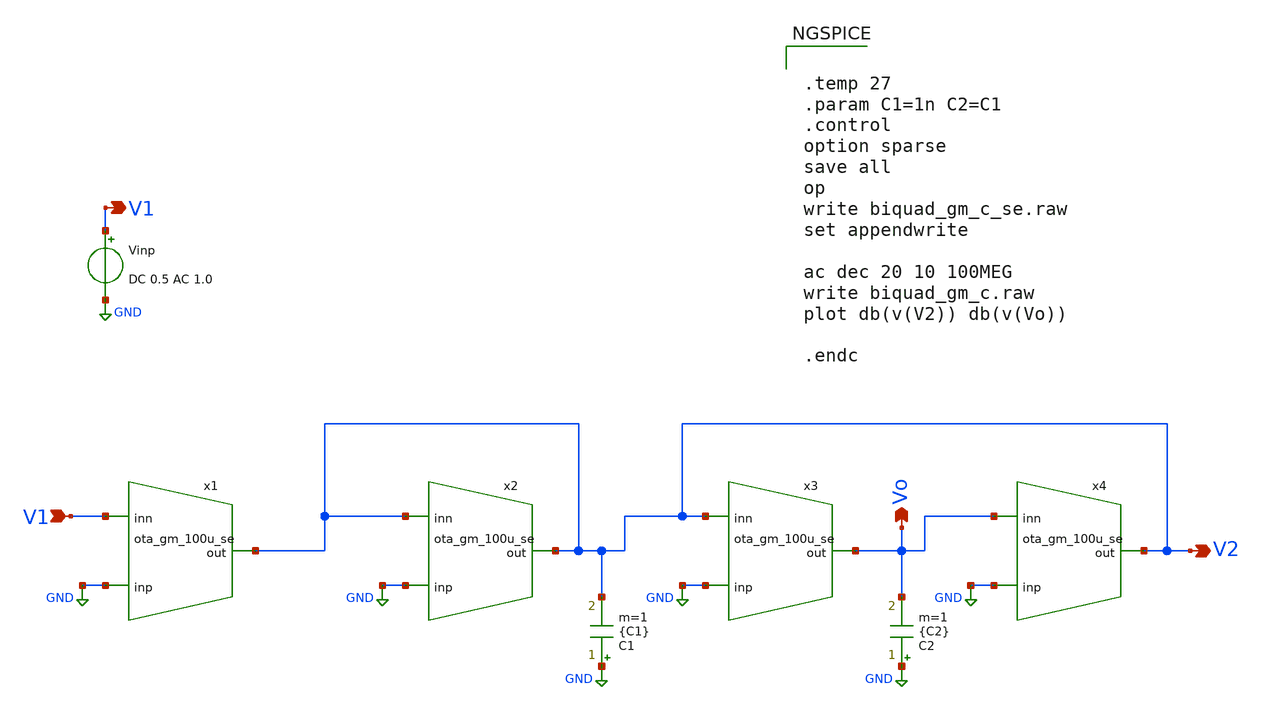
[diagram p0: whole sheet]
** sch_path: prj/template/2_Idealized_circuits/biquad_gm_c_se.sch
**.subckt biquad_gm_c_se V1 Vo V2 V1
*.ipin V1
*.opin Vo
*.opin V2
*.opin V1
C1 GND V2 {C1} m=1
C2 GND Vo {C2} m=1
x1 GND V1 V2 ota_gm_100u_se
x2 GND V2 V2 ota_gm_100u_se
x3 GND V2 Vo ota_gm_100u_se
x4 GND Vo V2 ota_gm_100u_se
Vinp V1 GND DC 0.5 AC 1.0
**** begin user architecture code


.temp 27
.param C1=1n C2=C1
.control
option sparse
save all
op
write biquad_gm_c_se.raw
set appendwrite

ac dec 20 10 100MEG
write biquad_gm_c.raw
plot db(v(V2)) db(v(Vo))

.endc


**** end user architecture code
**.ends

* expanding   symbol:  ota_gm_100u_se.sym # of pins=3
** sym_path: prj/template/2_Idealized_circuits/ota_gm_100u_se.sym
** sch_path: prj/template/2_Idealized_circuits/ota_gm_100u_se.sch
.subckt ota_gm_100u_se inp inn out
*.ipin inp
*.ipin inn
*.opin out
Co out GND 0.25p m=1
ro GND out 5MEG m=1
G1 out GND inp inn 200u
Ci inp inn 0.1p m=1
.ends

.GLOBAL GND
.end
